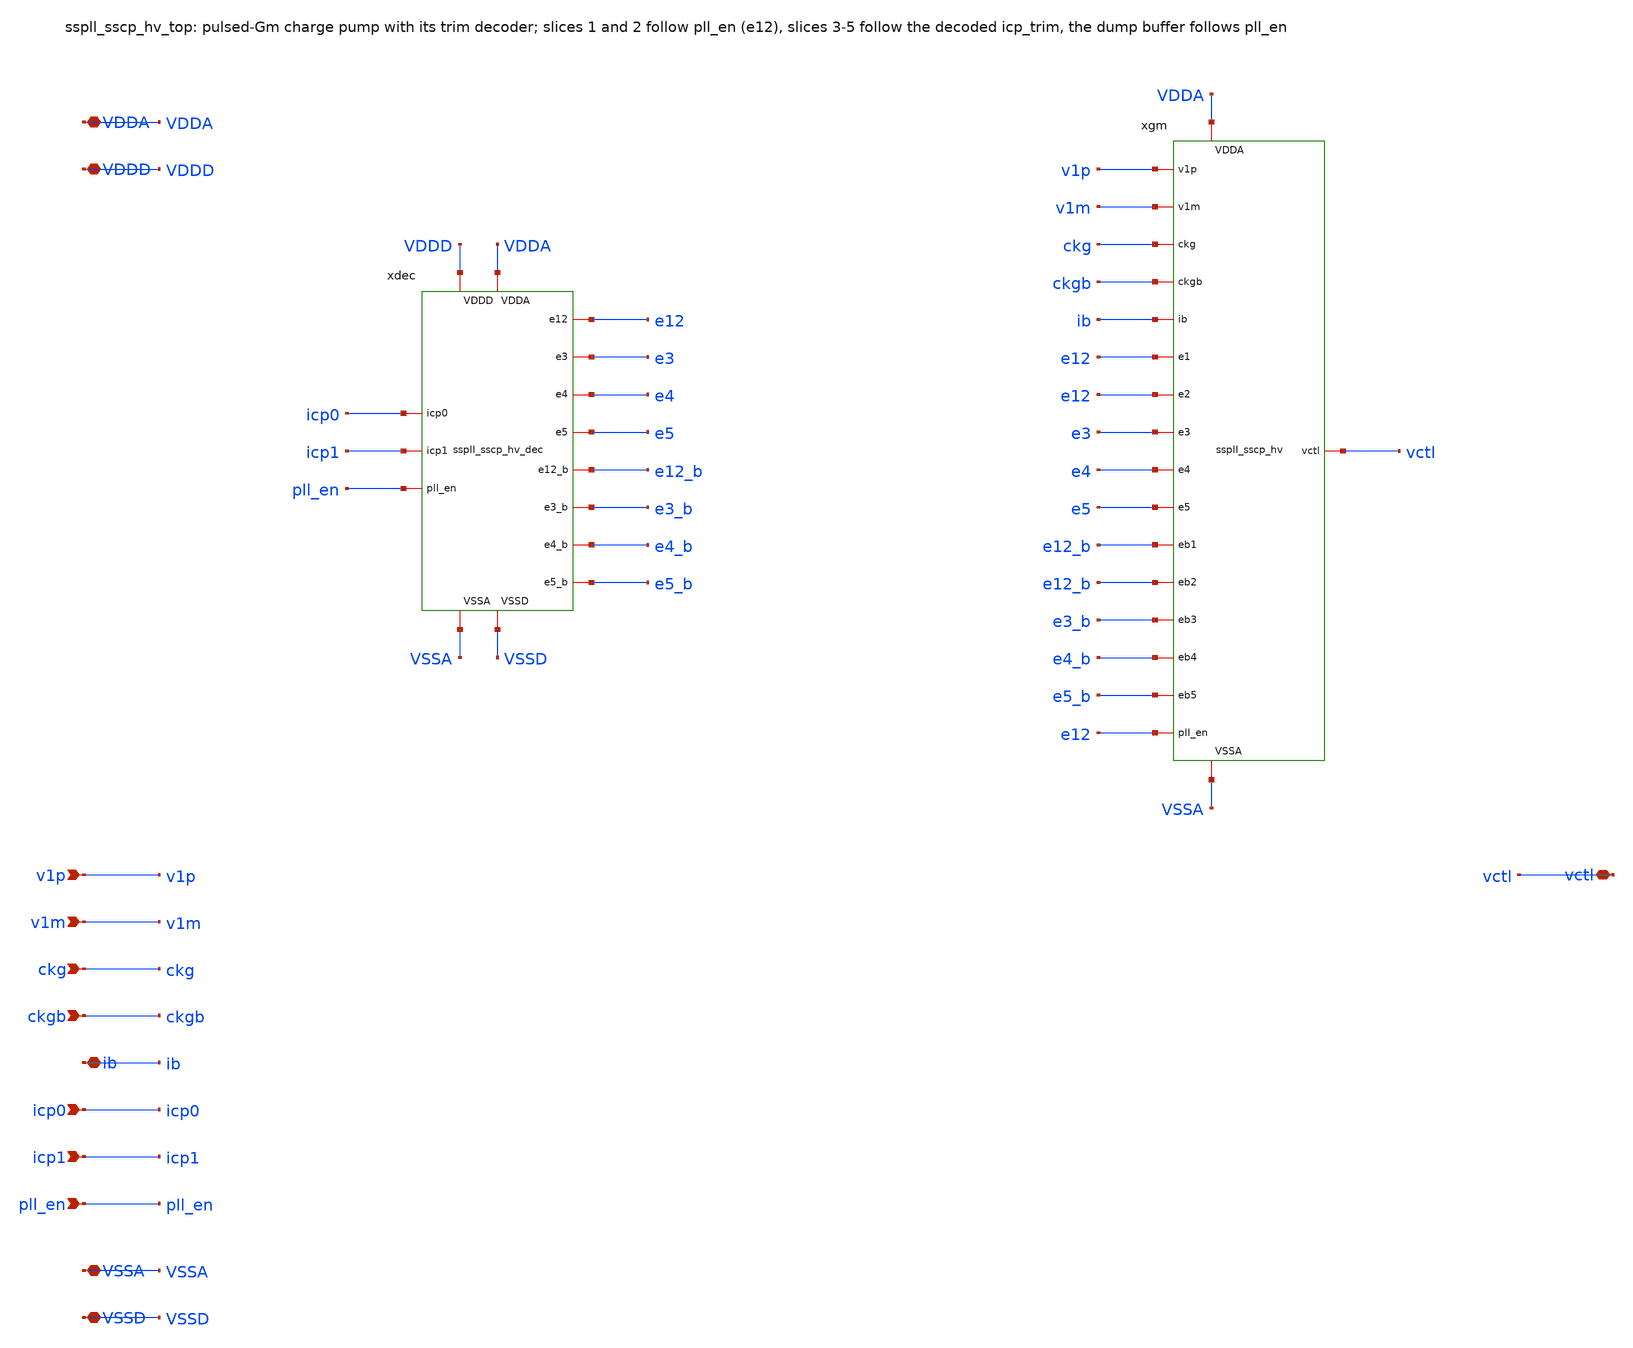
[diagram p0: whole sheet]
** sch_path: xschem/sscp_hv/sspll_sscp_hv_top.sch
**.subckt sspll_sscp_hv_top v1p v1m ckg ckgb ib icp0 icp1 pll_en vctl VDDA VDDD VSSA VSSD
*.ipin v1p
*.ipin v1m
*.ipin ckg
*.ipin ckgb
*.iopin ib
*.ipin icp0
*.ipin icp1
*.ipin pll_en
*.iopin vctl
*.iopin VDDA
*.iopin VDDD
*.iopin VSSA
*.iopin VSSD
xdec icp0 icp1 pll_en e12 e3 e4 e5 e12_b e3_b e4_b e5_b VDDD VDDA VSSA VSSD sspll_sscp_hv_dec
xgm v1p v1m ckg ckgb ib e12 e12 e3 e4 e5 e12_b e12_b e3_b e4_b e5_b e12 vctl VDDA VSSA sspll_sscp_hv
**.ends

* expanding   symbol:  sspll_sscp_hv_dec.sym # of pins=15
** sym_path: xschem/sscp_hv/sspll_sscp_hv_dec.sym
** sch_path: xschem/sscp_hv/sspll_sscp_hv_dec.sch
.subckt sspll_sscp_hv_dec icp0 icp1 pll_en e12 e3 e4 e5 e12_b e3_b e4_b e5_b VDDD VDDA VSSA VSSD
*.ipin icp0
*.ipin icp1
*.ipin pll_en
*.opin e12
*.opin e3
*.opin e4
*.opin e5
*.opin e12_b
*.opin e3_b
*.opin e4_b
*.opin e5_b
*.iopin VDDD
*.iopin VDDA
*.iopin VSSA
*.iopin VSSD
XXI0P c0b icp0 VDDD VDDD sky130_fd_pr__pfet_01v8 L=0.15 W=0.84 nf=1 ad='int((nf+1)/2) * W/nf * 0.29'
+ as='int((nf+2)/2) * W/nf * 0.29' pd='2*int((nf+1)/2) * (W/nf + 0.29)' ps='2*int((nf+2)/2) * (W/nf + 0.29)'
+ nrd='0.29 / W' nrs='0.29 / W' sa=0 sb=0 sd=0 mult=1 m=1
XXI0N c0b icp0 VSSD VSSD sky130_fd_pr__nfet_01v8 L=0.15 W=0.42 nf=1 ad='int((nf+1)/2) * W/nf * 0.29'
+ as='int((nf+2)/2) * W/nf * 0.29' pd='2*int((nf+1)/2) * (W/nf + 0.29)' ps='2*int((nf+2)/2) * (W/nf + 0.29)'
+ nrd='0.29 / W' nrs='0.29 / W' sa=0 sb=0 sd=0 mult=1 m=1
XXAPA a3 icp1 VDDD VDDD sky130_fd_pr__pfet_01v8 L=0.15 W=0.84 nf=1 ad='int((nf+1)/2) * W/nf * 0.29' as='int((nf+2)/2) * W/nf * 0.29'
+ pd='2*int((nf+1)/2) * (W/nf + 0.29)' ps='2*int((nf+2)/2) * (W/nf + 0.29)' nrd='0.29 / W' nrs='0.29 / W'
+ sa=0 sb=0 sd=0 mult=1 m=1
XXAPB a3 c0b VDDD VDDD sky130_fd_pr__pfet_01v8 L=0.15 W=0.84 nf=1 ad='int((nf+1)/2) * W/nf * 0.29' as='int((nf+2)/2) * W/nf * 0.29'
+ pd='2*int((nf+1)/2) * (W/nf + 0.29)' ps='2*int((nf+2)/2) * (W/nf + 0.29)' nrd='0.29 / W' nrs='0.29 / W'
+ sa=0 sb=0 sd=0 mult=1 m=1
XXANA a3 icp1 net1 VSSD sky130_fd_pr__nfet_01v8 L=0.15 W=0.84 nf=1 ad='int((nf+1)/2) * W/nf * 0.29' as='int((nf+2)/2) * W/nf * 0.29'
+ pd='2*int((nf+1)/2) * (W/nf + 0.29)' ps='2*int((nf+2)/2) * (W/nf + 0.29)' nrd='0.29 / W' nrs='0.29 / W'
+ sa=0 sb=0 sd=0 mult=1 m=1
XXANB net1 c0b VSSD VSSD sky130_fd_pr__nfet_01v8 L=0.15 W=0.84 nf=1 ad='int((nf+1)/2) * W/nf * 0.29'
+ as='int((nf+2)/2) * W/nf * 0.29' pd='2*int((nf+1)/2) * (W/nf + 0.29)' ps='2*int((nf+2)/2) * (W/nf + 0.29)'
+ nrd='0.29 / W' nrs='0.29 / W' sa=0 sb=0 sd=0 mult=1 m=1
XXBPA e3b pll_en VDDD VDDD sky130_fd_pr__pfet_01v8 L=0.15 W=0.84 nf=1 ad='int((nf+1)/2) * W/nf * 0.29'
+ as='int((nf+2)/2) * W/nf * 0.29' pd='2*int((nf+1)/2) * (W/nf + 0.29)' ps='2*int((nf+2)/2) * (W/nf + 0.29)'
+ nrd='0.29 / W' nrs='0.29 / W' sa=0 sb=0 sd=0 mult=1 m=1
XXBPB e3b a3 VDDD VDDD sky130_fd_pr__pfet_01v8 L=0.15 W=0.84 nf=1 ad='int((nf+1)/2) * W/nf * 0.29' as='int((nf+2)/2) * W/nf * 0.29'
+ pd='2*int((nf+1)/2) * (W/nf + 0.29)' ps='2*int((nf+2)/2) * (W/nf + 0.29)' nrd='0.29 / W' nrs='0.29 / W'
+ sa=0 sb=0 sd=0 mult=1 m=1
XXBNA e3b pll_en net2 VSSD sky130_fd_pr__nfet_01v8 L=0.15 W=0.84 nf=1 ad='int((nf+1)/2) * W/nf * 0.29'
+ as='int((nf+2)/2) * W/nf * 0.29' pd='2*int((nf+1)/2) * (W/nf + 0.29)' ps='2*int((nf+2)/2) * (W/nf + 0.29)'
+ nrd='0.29 / W' nrs='0.29 / W' sa=0 sb=0 sd=0 mult=1 m=1
XXBNB net2 a3 VSSD VSSD sky130_fd_pr__nfet_01v8 L=0.15 W=0.84 nf=1 ad='int((nf+1)/2) * W/nf * 0.29' as='int((nf+2)/2) * W/nf * 0.29'
+ pd='2*int((nf+1)/2) * (W/nf + 0.29)' ps='2*int((nf+2)/2) * (W/nf + 0.29)' nrd='0.29 / W' nrs='0.29 / W'
+ sa=0 sb=0 sd=0 mult=1 m=1
XXCPA e4b pll_en VDDD VDDD sky130_fd_pr__pfet_01v8 L=0.15 W=0.84 nf=1 ad='int((nf+1)/2) * W/nf * 0.29'
+ as='int((nf+2)/2) * W/nf * 0.29' pd='2*int((nf+1)/2) * (W/nf + 0.29)' ps='2*int((nf+2)/2) * (W/nf + 0.29)'
+ nrd='0.29 / W' nrs='0.29 / W' sa=0 sb=0 sd=0 mult=1 m=1
XXCPB e4b icp0 VDDD VDDD sky130_fd_pr__pfet_01v8 L=0.15 W=0.84 nf=1 ad='int((nf+1)/2) * W/nf * 0.29'
+ as='int((nf+2)/2) * W/nf * 0.29' pd='2*int((nf+1)/2) * (W/nf + 0.29)' ps='2*int((nf+2)/2) * (W/nf + 0.29)'
+ nrd='0.29 / W' nrs='0.29 / W' sa=0 sb=0 sd=0 mult=1 m=1
XXCNA e4b pll_en net3 VSSD sky130_fd_pr__nfet_01v8 L=0.15 W=0.84 nf=1 ad='int((nf+1)/2) * W/nf * 0.29'
+ as='int((nf+2)/2) * W/nf * 0.29' pd='2*int((nf+1)/2) * (W/nf + 0.29)' ps='2*int((nf+2)/2) * (W/nf + 0.29)'
+ nrd='0.29 / W' nrs='0.29 / W' sa=0 sb=0 sd=0 mult=1 m=1
XXCNB net3 icp0 VSSD VSSD sky130_fd_pr__nfet_01v8 L=0.15 W=0.84 nf=1 ad='int((nf+1)/2) * W/nf * 0.29'
+ as='int((nf+2)/2) * W/nf * 0.29' pd='2*int((nf+1)/2) * (W/nf + 0.29)' ps='2*int((nf+2)/2) * (W/nf + 0.29)'
+ nrd='0.29 / W' nrs='0.29 / W' sa=0 sb=0 sd=0 mult=1 m=1
XXDPA a5b icp1 VDDD VDDD sky130_fd_pr__pfet_01v8 L=0.15 W=0.84 nf=1 ad='int((nf+1)/2) * W/nf * 0.29'
+ as='int((nf+2)/2) * W/nf * 0.29' pd='2*int((nf+1)/2) * (W/nf + 0.29)' ps='2*int((nf+2)/2) * (W/nf + 0.29)'
+ nrd='0.29 / W' nrs='0.29 / W' sa=0 sb=0 sd=0 mult=1 m=1
XXDPB a5b icp0 VDDD VDDD sky130_fd_pr__pfet_01v8 L=0.15 W=0.84 nf=1 ad='int((nf+1)/2) * W/nf * 0.29'
+ as='int((nf+2)/2) * W/nf * 0.29' pd='2*int((nf+1)/2) * (W/nf + 0.29)' ps='2*int((nf+2)/2) * (W/nf + 0.29)'
+ nrd='0.29 / W' nrs='0.29 / W' sa=0 sb=0 sd=0 mult=1 m=1
XXDNA a5b icp1 net4 VSSD sky130_fd_pr__nfet_01v8 L=0.15 W=0.84 nf=1 ad='int((nf+1)/2) * W/nf * 0.29'
+ as='int((nf+2)/2) * W/nf * 0.29' pd='2*int((nf+1)/2) * (W/nf + 0.29)' ps='2*int((nf+2)/2) * (W/nf + 0.29)'
+ nrd='0.29 / W' nrs='0.29 / W' sa=0 sb=0 sd=0 mult=1 m=1
XXDNB net4 icp0 VSSD VSSD sky130_fd_pr__nfet_01v8 L=0.15 W=0.84 nf=1 ad='int((nf+1)/2) * W/nf * 0.29'
+ as='int((nf+2)/2) * W/nf * 0.29' pd='2*int((nf+1)/2) * (W/nf + 0.29)' ps='2*int((nf+2)/2) * (W/nf + 0.29)'
+ nrd='0.29 / W' nrs='0.29 / W' sa=0 sb=0 sd=0 mult=1 m=1
XXEPA e5b pll_en VDDD VDDD sky130_fd_pr__pfet_01v8 L=0.15 W=0.84 nf=1 ad='int((nf+1)/2) * W/nf * 0.29'
+ as='int((nf+2)/2) * W/nf * 0.29' pd='2*int((nf+1)/2) * (W/nf + 0.29)' ps='2*int((nf+2)/2) * (W/nf + 0.29)'
+ nrd='0.29 / W' nrs='0.29 / W' sa=0 sb=0 sd=0 mult=1 m=1
XXEPB e5b a5 VDDD VDDD sky130_fd_pr__pfet_01v8 L=0.15 W=0.84 nf=1 ad='int((nf+1)/2) * W/nf * 0.29' as='int((nf+2)/2) * W/nf * 0.29'
+ pd='2*int((nf+1)/2) * (W/nf + 0.29)' ps='2*int((nf+2)/2) * (W/nf + 0.29)' nrd='0.29 / W' nrs='0.29 / W'
+ sa=0 sb=0 sd=0 mult=1 m=1
XXENA e5b pll_en net5 VSSD sky130_fd_pr__nfet_01v8 L=0.15 W=0.84 nf=1 ad='int((nf+1)/2) * W/nf * 0.29'
+ as='int((nf+2)/2) * W/nf * 0.29' pd='2*int((nf+1)/2) * (W/nf + 0.29)' ps='2*int((nf+2)/2) * (W/nf + 0.29)'
+ nrd='0.29 / W' nrs='0.29 / W' sa=0 sb=0 sd=0 mult=1 m=1
XXENB net5 a5 VSSD VSSD sky130_fd_pr__nfet_01v8 L=0.15 W=0.84 nf=1 ad='int((nf+1)/2) * W/nf * 0.29' as='int((nf+2)/2) * W/nf * 0.29'
+ pd='2*int((nf+1)/2) * (W/nf + 0.29)' ps='2*int((nf+2)/2) * (W/nf + 0.29)' nrd='0.29 / W' nrs='0.29 / W'
+ sa=0 sb=0 sd=0 mult=1 m=1
XXI3P e3l e3b VDDD VDDD sky130_fd_pr__pfet_01v8 L=0.15 W=0.84 nf=1 ad='int((nf+1)/2) * W/nf * 0.29' as='int((nf+2)/2) * W/nf * 0.29'
+ pd='2*int((nf+1)/2) * (W/nf + 0.29)' ps='2*int((nf+2)/2) * (W/nf + 0.29)' nrd='0.29 / W' nrs='0.29 / W'
+ sa=0 sb=0 sd=0 mult=1 m=1
XXI3N e3l e3b VSSD VSSD sky130_fd_pr__nfet_01v8 L=0.15 W=0.42 nf=1 ad='int((nf+1)/2) * W/nf * 0.29' as='int((nf+2)/2) * W/nf * 0.29'
+ pd='2*int((nf+1)/2) * (W/nf + 0.29)' ps='2*int((nf+2)/2) * (W/nf + 0.29)' nrd='0.29 / W' nrs='0.29 / W'
+ sa=0 sb=0 sd=0 mult=1 m=1
XXI4P e4l e4b VDDD VDDD sky130_fd_pr__pfet_01v8 L=0.15 W=0.84 nf=1 ad='int((nf+1)/2) * W/nf * 0.29' as='int((nf+2)/2) * W/nf * 0.29'
+ pd='2*int((nf+1)/2) * (W/nf + 0.29)' ps='2*int((nf+2)/2) * (W/nf + 0.29)' nrd='0.29 / W' nrs='0.29 / W'
+ sa=0 sb=0 sd=0 mult=1 m=1
XXI4N e4l e4b VSSD VSSD sky130_fd_pr__nfet_01v8 L=0.15 W=0.42 nf=1 ad='int((nf+1)/2) * W/nf * 0.29' as='int((nf+2)/2) * W/nf * 0.29'
+ pd='2*int((nf+1)/2) * (W/nf + 0.29)' ps='2*int((nf+2)/2) * (W/nf + 0.29)' nrd='0.29 / W' nrs='0.29 / W'
+ sa=0 sb=0 sd=0 mult=1 m=1
XXI5P a5 a5b VDDD VDDD sky130_fd_pr__pfet_01v8 L=0.15 W=0.84 nf=1 ad='int((nf+1)/2) * W/nf * 0.29' as='int((nf+2)/2) * W/nf * 0.29'
+ pd='2*int((nf+1)/2) * (W/nf + 0.29)' ps='2*int((nf+2)/2) * (W/nf + 0.29)' nrd='0.29 / W' nrs='0.29 / W'
+ sa=0 sb=0 sd=0 mult=1 m=1
XXI5N a5 a5b VSSD VSSD sky130_fd_pr__nfet_01v8 L=0.15 W=0.42 nf=1 ad='int((nf+1)/2) * W/nf * 0.29' as='int((nf+2)/2) * W/nf * 0.29'
+ pd='2*int((nf+1)/2) * (W/nf + 0.29)' ps='2*int((nf+2)/2) * (W/nf + 0.29)' nrd='0.29 / W' nrs='0.29 / W'
+ sa=0 sb=0 sd=0 mult=1 m=1
XXI6P e5l e5b VDDD VDDD sky130_fd_pr__pfet_01v8 L=0.15 W=0.84 nf=1 ad='int((nf+1)/2) * W/nf * 0.29' as='int((nf+2)/2) * W/nf * 0.29'
+ pd='2*int((nf+1)/2) * (W/nf + 0.29)' ps='2*int((nf+2)/2) * (W/nf + 0.29)' nrd='0.29 / W' nrs='0.29 / W'
+ sa=0 sb=0 sd=0 mult=1 m=1
XXI6N e5l e5b VSSD VSSD sky130_fd_pr__nfet_01v8 L=0.15 W=0.42 nf=1 ad='int((nf+1)/2) * W/nf * 0.29' as='int((nf+2)/2) * W/nf * 0.29'
+ pd='2*int((nf+1)/2) * (W/nf + 0.29)' ps='2*int((nf+2)/2) * (W/nf + 0.29)' nrd='0.29 / W' nrs='0.29 / W'
+ sa=0 sb=0 sd=0 mult=1 m=1
xlse12 pll_en e12 e12_b VDDD VDDA VSSA VSSD sspll_ls_1v8_3v3
xlse3 e3l e3 e3_b VDDD VDDA VSSA VSSD sspll_ls_1v8_3v3
xlse4 e4l e4 e4_b VDDD VDDA VSSA VSSD sspll_ls_1v8_3v3
xlse5 e5l e5 e5_b VDDD VDDA VSSA VSSD sspll_ls_1v8_3v3
.ends


* expanding   symbol:  sspll_sscp_hv.sym # of pins=19
** sym_path: xschem/sscp_hv/sspll_sscp_hv.sym
** sch_path: xschem/sscp_hv/sspll_sscp_hv.sch
.subckt sspll_sscp_hv v1p v1m ckg ckgb ib e1 e2 e3 e4 e5 eb1 eb2 eb3 eb4 eb5 pll_en vctl VDDA VSSA
*.iopin vctl
*.ipin v1p
*.ipin v1m
*.ipin ckg
*.ipin ckgb
*.iopin ib
*.ipin e1
*.ipin e2
*.ipin e3
*.ipin e4
*.ipin e5
*.ipin eb1
*.ipin eb2
*.ipin eb3
*.ipin eb4
*.ipin eb5
*.ipin pll_en
*.iopin VDDA
*.iopin VSSA
xs1 v1p v1m ib pb e1 eb1 net1 vdump VDDA VSSA sspll_sscp_hv_slice
xs2 v1p v1m ib pb e2 eb2 net1 vdump VDDA VSSA sspll_sscp_hv_slice
xs3 v1p v1m ib pb e3 eb3 net1 vdump VDDA VSSA sspll_sscp_hv_slice
xs4 v1p v1m ib pb e4 eb4 net1 vdump VDDA VSSA sspll_sscp_hv_slice
xs5 v1p v1m ib pb e5 eb5 net1 vdump VDDA VSSA sspll_sscp_hv_slice
xtf net1 ckg ckgb vctl VDDA VSSA sspll_sscp_hv_tg
xtd net1 ckgb ckg vdump VDDA VSSA sspll_sscp_hv_tg
xbuf vctl ib pll_en vdump VDDA VSSA sspll_sscp_hv_buf
XXCDUMP vdump VSSA sky130_fd_pr__cap_mim_m3_1 W=22.4 L=22.4 MF=2 m=2
XXNB ib ib VSSA VSSA sky130_fd_pr__nfet_g5v0d10v5 L=8.0 W=1 nf=1 ad='int((nf+1)/2) * W/nf * 0.29' as='int((nf+2)/2) * W/nf * 0.29'
+ pd='2*int((nf+1)/2) * (W/nf + 0.29)' ps='2*int((nf+2)/2) * (W/nf + 0.29)' nrd='0.29 / W' nrs='0.29 / W'
+ sa=0 sb=0 sd=0 mult=1 m=1
XXRPE net2 VSSA VDDA VDDA sky130_fd_pr__pfet_g5v0d10v5 L=0.5 W=2 nf=1 ad='int((nf+1)/2) * W/nf * 0.29'
+ as='int((nf+2)/2) * W/nf * 0.29' pd='2*int((nf+1)/2) * (W/nf + 0.29)' ps='2*int((nf+2)/2) * (W/nf + 0.29)'
+ nrd='0.29 / W' nrs='0.29 / W' sa=0 sb=0 sd=0 mult=12 m=12
XXRP pb pb net2 VDDA sky130_fd_pr__pfet_g5v0d10v5 L=4.0 W=4 nf=1 ad='int((nf+1)/2) * W/nf * 0.29' as='int((nf+2)/2) * W/nf * 0.29'
+ pd='2*int((nf+1)/2) * (W/nf + 0.29)' ps='2*int((nf+2)/2) * (W/nf + 0.29)' nrd='0.29 / W' nrs='0.29 / W'
+ sa=0 sb=0 sd=0 mult=12 m=12
XXRD pb net5 net3 VSSA sky130_fd_pr__nfet_g5v0d10v5 L=1.0 W=4 nf=1 ad='int((nf+1)/2) * W/nf * 0.29' as='int((nf+2)/2) * W/nf * 0.29'
+ pd='2*int((nf+1)/2) * (W/nf + 0.29)' ps='2*int((nf+2)/2) * (W/nf + 0.29)' nrd='0.29 / W' nrs='0.29 / W'
+ sa=0 sb=0 sd=0 mult=6 m=6
XXRE net3 pll_en net4 VSSA sky130_fd_pr__nfet_g5v0d10v5 L=0.5 W=1 nf=1 ad='int((nf+1)/2) * W/nf * 0.29'
+ as='int((nf+2)/2) * W/nf * 0.29' pd='2*int((nf+1)/2) * (W/nf + 0.29)' ps='2*int((nf+2)/2) * (W/nf + 0.29)'
+ nrd='0.29 / W' nrs='0.29 / W' sa=0 sb=0 sd=0 mult=12 m=12
XXRT net4 ib VSSA VSSA sky130_fd_pr__nfet_g5v0d10v5 L=8.0 W=1 nf=1 ad='int((nf+1)/2) * W/nf * 0.29' as='int((nf+2)/2) * W/nf * 0.29'
+ pd='2*int((nf+1)/2) * (W/nf + 0.29)' ps='2*int((nf+2)/2) * (W/nf + 0.29)' nrd='0.29 / W' nrs='0.29 / W'
+ sa=0 sb=0 sd=0 mult=12 m=12
XXRC1 net5 VDDA VSSA sky130_fd_pr__res_xhigh_po_0p35 L=150.0 mult=1 m=1
XXRC2 VSSA net5 VSSA sky130_fd_pr__res_xhigh_po_0p35 L=150.0 mult=1 m=1
.ends


* expanding   symbol:  ../cco_hv/sspll_ls_1v8_3v3.sym # of pins=7
** sym_path: xschem/cco_hv/sspll_ls_1v8_3v3.sym
** sch_path: xschem/cco_hv/sspll_ls_1v8_3v3.sch
.subckt sspll_ls_1v8_3v3 in out outb VDDD VDDA VSSA VSSD
*.iopin VDDD
*.iopin VDDA
*.iopin VSSD
*.iopin VSSA
*.ipin in
*.opin outb
*.opin out
XXPI net1 in VDDD VDDD sky130_fd_pr__pfet_01v8 L=0.15 W=1 nf=1 ad='int((nf+1)/2) * W/nf * 0.29' as='int((nf+2)/2) * W/nf * 0.29'
+ pd='2*int((nf+1)/2) * (W/nf + 0.29)' ps='2*int((nf+2)/2) * (W/nf + 0.29)' nrd='0.29 / W' nrs='0.29 / W'
+ sa=0 sb=0 sd=0 mult=1 m=1
XXNI net1 in VSSD VSSD sky130_fd_pr__nfet_01v8 L=0.15 W=0.5 nf=1 ad='int((nf+1)/2) * W/nf * 0.29' as='int((nf+2)/2) * W/nf * 0.29'
+ pd='2*int((nf+1)/2) * (W/nf + 0.29)' ps='2*int((nf+2)/2) * (W/nf + 0.29)' nrd='0.29 / W' nrs='0.29 / W'
+ sa=0 sb=0 sd=0 mult=1 m=1
XXP1 net2 net3 VDDA VDDA sky130_fd_pr__pfet_g5v0d10v5 L=0.5 W=1 nf=1 ad='int((nf+1)/2) * W/nf * 0.29'
+ as='int((nf+2)/2) * W/nf * 0.29' pd='2*int((nf+1)/2) * (W/nf + 0.29)' ps='2*int((nf+2)/2) * (W/nf + 0.29)'
+ nrd='0.29 / W' nrs='0.29 / W' sa=0 sb=0 sd=0 mult=1 m=1
XXP2 net3 net2 VDDA VDDA sky130_fd_pr__pfet_g5v0d10v5 L=0.5 W=1 nf=1 ad='int((nf+1)/2) * W/nf * 0.29'
+ as='int((nf+2)/2) * W/nf * 0.29' pd='2*int((nf+1)/2) * (W/nf + 0.29)' ps='2*int((nf+2)/2) * (W/nf + 0.29)'
+ nrd='0.29 / W' nrs='0.29 / W' sa=0 sb=0 sd=0 mult=1 m=1
XXN1 net2 in VSSA VSSA sky130_fd_pr__nfet_g5v0d10v5 L=0.5 W=3 nf=1 ad='int((nf+1)/2) * W/nf * 0.29' as='int((nf+2)/2) * W/nf * 0.29'
+ pd='2*int((nf+1)/2) * (W/nf + 0.29)' ps='2*int((nf+2)/2) * (W/nf + 0.29)' nrd='0.29 / W' nrs='0.29 / W'
+ sa=0 sb=0 sd=0 mult=1 m=1
XXN2 net3 net1 VSSA VSSA sky130_fd_pr__nfet_g5v0d10v5 L=0.5 W=3 nf=1 ad='int((nf+1)/2) * W/nf * 0.29'
+ as='int((nf+2)/2) * W/nf * 0.29' pd='2*int((nf+1)/2) * (W/nf + 0.29)' ps='2*int((nf+2)/2) * (W/nf + 0.29)'
+ nrd='0.29 / W' nrs='0.29 / W' sa=0 sb=0 sd=0 mult=1 m=1
XXPB outb net3 VDDA VDDA sky130_fd_pr__pfet_g5v0d10v5 L=0.5 W=2 nf=1 ad='int((nf+1)/2) * W/nf * 0.29'
+ as='int((nf+2)/2) * W/nf * 0.29' pd='2*int((nf+1)/2) * (W/nf + 0.29)' ps='2*int((nf+2)/2) * (W/nf + 0.29)'
+ nrd='0.29 / W' nrs='0.29 / W' sa=0 sb=0 sd=0 mult=1 m=1
XXNB outb net3 VSSA VSSA sky130_fd_pr__nfet_g5v0d10v5 L=0.5 W=1 nf=1 ad='int((nf+1)/2) * W/nf * 0.29'
+ as='int((nf+2)/2) * W/nf * 0.29' pd='2*int((nf+1)/2) * (W/nf + 0.29)' ps='2*int((nf+2)/2) * (W/nf + 0.29)'
+ nrd='0.29 / W' nrs='0.29 / W' sa=0 sb=0 sd=0 mult=1 m=1
XXPO out net2 VDDA VDDA sky130_fd_pr__pfet_g5v0d10v5 L=0.5 W=2 nf=1 ad='int((nf+1)/2) * W/nf * 0.29'
+ as='int((nf+2)/2) * W/nf * 0.29' pd='2*int((nf+1)/2) * (W/nf + 0.29)' ps='2*int((nf+2)/2) * (W/nf + 0.29)'
+ nrd='0.29 / W' nrs='0.29 / W' sa=0 sb=0 sd=0 mult=1 m=1
XXNO out net2 VSSA VSSA sky130_fd_pr__nfet_g5v0d10v5 L=0.5 W=1 nf=1 ad='int((nf+1)/2) * W/nf * 0.29'
+ as='int((nf+2)/2) * W/nf * 0.29' pd='2*int((nf+1)/2) * (W/nf + 0.29)' ps='2*int((nf+2)/2) * (W/nf + 0.29)'
+ nrd='0.29 / W' nrs='0.29 / W' sa=0 sb=0 sd=0 mult=1 m=1
.ends


* expanding   symbol:  sspll_sscp_hv_slice.sym # of pins=10
** sym_path: xschem/sscp_hv/sspll_sscp_hv_slice.sym
** sch_path: xschem/sscp_hv/sspll_sscp_hv_slice.sch
.subckt sspll_sscp_hv_slice v1p v1m nb pb en enb x xc VDDA VSSA
*.ipin v1p
*.ipin v1m
*.ipin nb
*.ipin pb
*.ipin en
*.ipin enb
*.iopin x
*.iopin xc
*.iopin VDDA
*.iopin VSSA
XXPE1 net1 enb VDDA VDDA sky130_fd_pr__pfet_g5v0d10v5 L=0.5 W=2 nf=1 ad='int((nf+1)/2) * W/nf * 0.29'
+ as='int((nf+2)/2) * W/nf * 0.29' pd='2*int((nf+1)/2) * (W/nf + 0.29)' ps='2*int((nf+2)/2) * (W/nf + 0.29)'
+ nrd='0.29 / W' nrs='0.29 / W' sa=0 sb=0 sd=0 mult=2 m=2
XXPE2 net2 enb VDDA VDDA sky130_fd_pr__pfet_g5v0d10v5 L=0.5 W=2 nf=1 ad='int((nf+1)/2) * W/nf * 0.29'
+ as='int((nf+2)/2) * W/nf * 0.29' pd='2*int((nf+1)/2) * (W/nf + 0.29)' ps='2*int((nf+2)/2) * (W/nf + 0.29)'
+ nrd='0.29 / W' nrs='0.29 / W' sa=0 sb=0 sd=0 mult=2 m=2
XXPC xc pb net1 VDDA sky130_fd_pr__pfet_g5v0d10v5 L=4.0 W=4 nf=1 ad='int((nf+1)/2) * W/nf * 0.29' as='int((nf+2)/2) * W/nf * 0.29'
+ pd='2*int((nf+1)/2) * (W/nf + 0.29)' ps='2*int((nf+2)/2) * (W/nf + 0.29)' nrd='0.29 / W' nrs='0.29 / W'
+ sa=0 sb=0 sd=0 mult=2 m=2
XXPX x pb net2 VDDA sky130_fd_pr__pfet_g5v0d10v5 L=4.0 W=4 nf=1 ad='int((nf+1)/2) * W/nf * 0.29' as='int((nf+2)/2) * W/nf * 0.29'
+ pd='2*int((nf+1)/2) * (W/nf + 0.29)' ps='2*int((nf+2)/2) * (W/nf + 0.29)' nrd='0.29 / W' nrs='0.29 / W'
+ sa=0 sb=0 sd=0 mult=2 m=2
XXN1 xc v1p net3 VSSA sky130_fd_pr__nfet_g5v0d10v5 L=1.0 W=4 nf=1 ad='int((nf+1)/2) * W/nf * 0.29' as='int((nf+2)/2) * W/nf * 0.29'
+ pd='2*int((nf+1)/2) * (W/nf + 0.29)' ps='2*int((nf+2)/2) * (W/nf + 0.29)' nrd='0.29 / W' nrs='0.29 / W'
+ sa=0 sb=0 sd=0 mult=1 m=1
XXN2 x v1m net4 VSSA sky130_fd_pr__nfet_g5v0d10v5 L=1.0 W=4 nf=1 ad='int((nf+1)/2) * W/nf * 0.29' as='int((nf+2)/2) * W/nf * 0.29'
+ pd='2*int((nf+1)/2) * (W/nf + 0.29)' ps='2*int((nf+2)/2) * (W/nf + 0.29)' nrd='0.29 / W' nrs='0.29 / W'
+ sa=0 sb=0 sd=0 mult=1 m=1
xrs net3 net4 VSSA sspll_sscp_hv_rs
XXE1 net3 en net5 VSSA sky130_fd_pr__nfet_g5v0d10v5 L=0.5 W=1 nf=1 ad='int((nf+1)/2) * W/nf * 0.29' as='int((nf+2)/2) * W/nf * 0.29'
+ pd='2*int((nf+1)/2) * (W/nf + 0.29)' ps='2*int((nf+2)/2) * (W/nf + 0.29)' nrd='0.29 / W' nrs='0.29 / W'
+ sa=0 sb=0 sd=0 mult=2 m=2
XXE2 net4 en net6 VSSA sky130_fd_pr__nfet_g5v0d10v5 L=0.5 W=1 nf=1 ad='int((nf+1)/2) * W/nf * 0.29' as='int((nf+2)/2) * W/nf * 0.29'
+ pd='2*int((nf+1)/2) * (W/nf + 0.29)' ps='2*int((nf+2)/2) * (W/nf + 0.29)' nrd='0.29 / W' nrs='0.29 / W'
+ sa=0 sb=0 sd=0 mult=2 m=2
XXT1 net5 nb VSSA VSSA sky130_fd_pr__nfet_g5v0d10v5 L=8.0 W=1 nf=1 ad='int((nf+1)/2) * W/nf * 0.29' as='int((nf+2)/2) * W/nf * 0.29'
+ pd='2*int((nf+1)/2) * (W/nf + 0.29)' ps='2*int((nf+2)/2) * (W/nf + 0.29)' nrd='0.29 / W' nrs='0.29 / W'
+ sa=0 sb=0 sd=0 mult=2 m=2
XXT2 net6 nb VSSA VSSA sky130_fd_pr__nfet_g5v0d10v5 L=8.0 W=1 nf=1 ad='int((nf+1)/2) * W/nf * 0.29' as='int((nf+2)/2) * W/nf * 0.29'
+ pd='2*int((nf+1)/2) * (W/nf + 0.29)' ps='2*int((nf+2)/2) * (W/nf + 0.29)' nrd='0.29 / W' nrs='0.29 / W'
+ sa=0 sb=0 sd=0 mult=2 m=2
.ends


* expanding   symbol:  sspll_sscp_hv_tg.sym # of pins=6
** sym_path: xschem/sscp_hv/sspll_sscp_hv_tg.sym
** sch_path: xschem/sscp_hv/sspll_sscp_hv_tg.sch
.subckt sspll_sscp_hv_tg a g gb b VDDA VSSA
*.iopin a
*.iopin b
*.ipin g
*.ipin gb
*.iopin VDDA
*.iopin VSSA
XXN a g b VSSA sky130_fd_pr__nfet_g5v0d10v5 L=0.5 W=1 nf=1 ad='int((nf+1)/2) * W/nf * 0.29' as='int((nf+2)/2) * W/nf * 0.29'
+ pd='2*int((nf+1)/2) * (W/nf + 0.29)' ps='2*int((nf+2)/2) * (W/nf + 0.29)' nrd='0.29 / W' nrs='0.29 / W'
+ sa=0 sb=0 sd=0 mult=1 m=1
XXP b gb a VDDA sky130_fd_pr__pfet_g5v0d10v5 L=0.5 W=1 nf=1 ad='int((nf+1)/2) * W/nf * 0.29' as='int((nf+2)/2) * W/nf * 0.29'
+ pd='2*int((nf+1)/2) * (W/nf + 0.29)' ps='2*int((nf+2)/2) * (W/nf + 0.29)' nrd='0.29 / W' nrs='0.29 / W'
+ sa=0 sb=0 sd=0 mult=1 m=1
.ends


* expanding   symbol:  sspll_sscp_hv_buf.sym # of pins=6
** sym_path: xschem/sscp_hv/sspll_sscp_hv_buf.sym
** sch_path: xschem/sscp_hv/sspll_sscp_hv_buf.sch
.subckt sspll_sscp_hv_buf inp nb en out VDDA VSS
*.ipin inp
*.ipin nb
*.ipin en
*.opin out
*.iopin VDDA
*.iopin VSS
XXL1 o1 o1 VDDA VDDA sky130_fd_pr__pfet_g5v0d10v5 L=2.0 W=16 nf=1 ad='int((nf+1)/2) * W/nf * 0.29' as='int((nf+2)/2) * W/nf * 0.29'
+ pd='2*int((nf+1)/2) * (W/nf + 0.29)' ps='2*int((nf+2)/2) * (W/nf + 0.29)' nrd='0.29 / W' nrs='0.29 / W'
+ sa=0 sb=0 sd=0 mult=1 m=1
XXL2 out o1 VDDA VDDA sky130_fd_pr__pfet_g5v0d10v5 L=2.0 W=16 nf=1 ad='int((nf+1)/2) * W/nf * 0.29' as='int((nf+2)/2) * W/nf * 0.29'
+ pd='2*int((nf+1)/2) * (W/nf + 0.29)' ps='2*int((nf+2)/2) * (W/nf + 0.29)' nrd='0.29 / W' nrs='0.29 / W'
+ sa=0 sb=0 sd=0 mult=1 m=1
XXA1 o1 inp net1 VSS sky130_fd_pr__nfet_g5v0d10v5 L=2.0 W=8 nf=1 ad='int((nf+1)/2) * W/nf * 0.29' as='int((nf+2)/2) * W/nf * 0.29'
+ pd='2*int((nf+1)/2) * (W/nf + 0.29)' ps='2*int((nf+2)/2) * (W/nf + 0.29)' nrd='0.29 / W' nrs='0.29 / W'
+ sa=0 sb=0 sd=0 mult=1 m=1
XXA2 out out net1 VSS sky130_fd_pr__nfet_g5v0d10v5 L=2.0 W=8 nf=1 ad='int((nf+1)/2) * W/nf * 0.29' as='int((nf+2)/2) * W/nf * 0.29'
+ pd='2*int((nf+1)/2) * (W/nf + 0.29)' ps='2*int((nf+2)/2) * (W/nf + 0.29)' nrd='0.29 / W' nrs='0.29 / W'
+ sa=0 sb=0 sd=0 mult=1 m=1
XXBE net1 en net2 VSS sky130_fd_pr__nfet_g5v0d10v5 L=0.5 W=1 nf=1 ad='int((nf+1)/2) * W/nf * 0.29' as='int((nf+2)/2) * W/nf * 0.29'
+ pd='2*int((nf+1)/2) * (W/nf + 0.29)' ps='2*int((nf+2)/2) * (W/nf + 0.29)' nrd='0.29 / W' nrs='0.29 / W'
+ sa=0 sb=0 sd=0 mult=10 m=10
XXBT net2 nb VSS VSS sky130_fd_pr__nfet_g5v0d10v5 L=8.0 W=2 nf=1 ad='int((nf+1)/2) * W/nf * 0.29' as='int((nf+2)/2) * W/nf * 0.29'
+ pd='2*int((nf+1)/2) * (W/nf + 0.29)' ps='2*int((nf+2)/2) * (W/nf + 0.29)' nrd='0.29 / W' nrs='0.29 / W'
+ sa=0 sb=0 sd=0 mult=10 m=10
.ends


* expanding   symbol:  sspll_sscp_hv_rs.sym # of pins=3
** sym_path: xschem/sscp_hv/sspll_sscp_hv_rs.sym
** sch_path: xschem/sscp_hv/sspll_sscp_hv_rs.sch
.subckt sspll_sscp_hv_rs a b VSS
*.iopin a
*.iopin b
*.iopin VSS
XXR0 b a VSS sky130_fd_pr__res_xhigh_po_0p35 L=17.2 mult=1 m=1
.ends

.end
